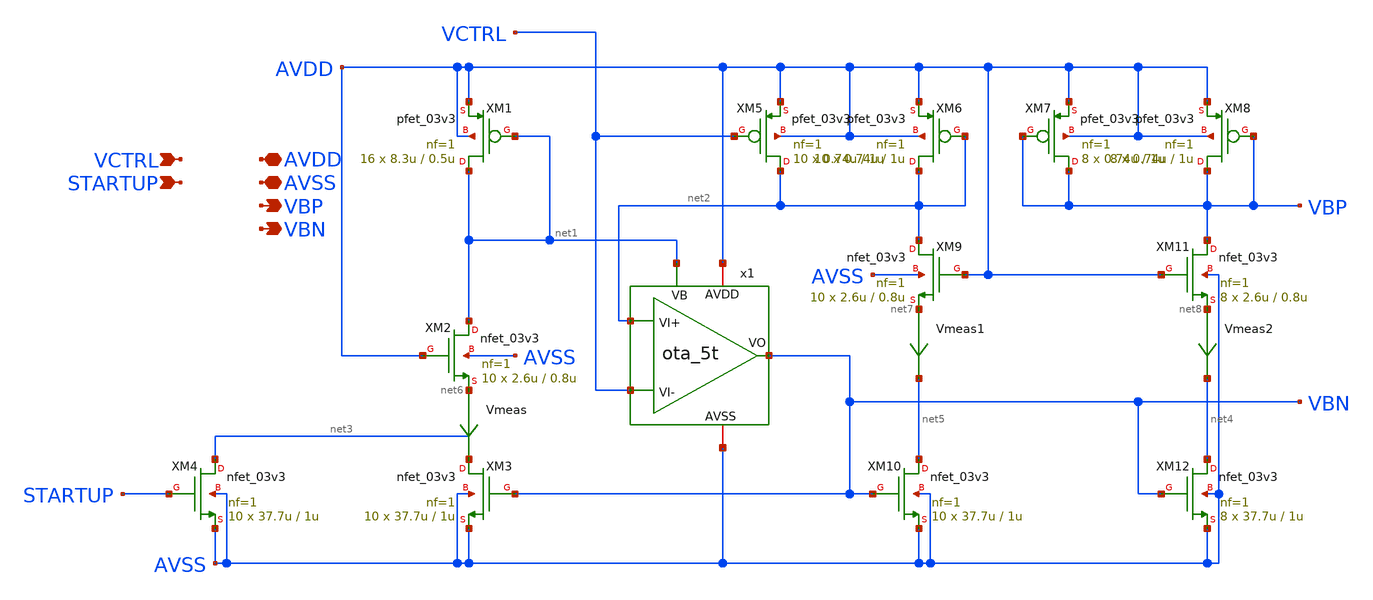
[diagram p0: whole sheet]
** sch_path: designs/libs/core_analog/bias_generator/bias_generator.sch
**.subckt bias_generator VCTRL STARTUP AVDD AVSS VBP VBN
*.ipin VCTRL
*.ipin STARTUP
*.iopin AVDD
*.iopin AVSS
*.opin VBP
*.opin VBN
x1 VBN AVDD net2 VCTRL AVSS net1 ota_5t
XM1 net1 net1 AVDD AVDD pfet_03v3 L=0.5u W=8.3u nf=1 ad='int((nf+1)/2) * W/nf * 0.18u' as='int((nf+2)/2) * W/nf * 0.18u'
+ pd='2*int((nf+1)/2) * (W/nf + 0.18u)' ps='2*int((nf+2)/2) * (W/nf + 0.18u)' nrd='0.18u / W' nrs='0.18u / W'
+ sa=0 sb=0 sd=0 m=16
Vmeas net6 net3 0
.save i(vmeas)
Vmeas1 net7 net5 0
.save i(vmeas1)
Vmeas2 net8 net4 0
.save i(vmeas2)
XM10 net5 VBN AVSS AVSS nfet_03v3 L=1u W=37.7u nf=1 ad='int((nf+1)/2) * W/nf * 0.18u' as='int((nf+2)/2) * W/nf * 0.18u'
+ pd='2*int((nf+1)/2) * (W/nf + 0.18u)' ps='2*int((nf+2)/2) * (W/nf + 0.18u)' nrd='0.18u / W' nrs='0.18u / W'
+ sa=0 sb=0 sd=0 m=10
XM5 net2 VCTRL AVDD AVDD pfet_03v3 L=1u W=0.74u nf=1 ad='int((nf+1)/2) * W/nf * 0.18u' as='int((nf+2)/2) * W/nf * 0.18u'
+ pd='2*int((nf+1)/2) * (W/nf + 0.18u)' ps='2*int((nf+2)/2) * (W/nf + 0.18u)' nrd='0.18u / W' nrs='0.18u / W'
+ sa=0 sb=0 sd=0 m=10
XM9 net2 AVDD net7 AVSS nfet_03v3 L=0.8u W=2.6u nf=1 ad='int((nf+1)/2) * W/nf * 0.18u' as='int((nf+2)/2) * W/nf * 0.18u'
+ pd='2*int((nf+1)/2) * (W/nf + 0.18u)' ps='2*int((nf+2)/2) * (W/nf + 0.18u)' nrd='0.18u / W' nrs='0.18u / W'
+ sa=0 sb=0 sd=0 m=10
XM11 VBP AVDD net8 AVSS nfet_03v3 L=0.8u W=2.6u nf=1 ad='int((nf+1)/2) * W/nf * 0.18u' as='int((nf+2)/2) * W/nf * 0.18u'
+ pd='2*int((nf+1)/2) * (W/nf + 0.18u)' ps='2*int((nf+2)/2) * (W/nf + 0.18u)' nrd='0.18u / W' nrs='0.18u / W'
+ sa=0 sb=0 sd=0 m=8
XM6 net2 net2 AVDD AVDD pfet_03v3 L=1u W=0.74u nf=1 ad='int((nf+1)/2) * W/nf * 0.18u' as='int((nf+2)/2) * W/nf * 0.18u'
+ pd='2*int((nf+1)/2) * (W/nf + 0.18u)' ps='2*int((nf+2)/2) * (W/nf + 0.18u)' nrd='0.18u / W' nrs='0.18u / W'
+ sa=0 sb=0 sd=0 m=10
XM7 VBP VBP AVDD AVDD pfet_03v3 L=1u W=0.74u nf=1 ad='int((nf+1)/2) * W/nf * 0.18u' as='int((nf+2)/2) * W/nf * 0.18u'
+ pd='2*int((nf+1)/2) * (W/nf + 0.18u)' ps='2*int((nf+2)/2) * (W/nf + 0.18u)' nrd='0.18u / W' nrs='0.18u / W'
+ sa=0 sb=0 sd=0 m=8
XM8 VBP VBP AVDD AVDD pfet_03v3 L=1u W=0.74u nf=1 ad='int((nf+1)/2) * W/nf * 0.18u' as='int((nf+2)/2) * W/nf * 0.18u'
+ pd='2*int((nf+1)/2) * (W/nf + 0.18u)' ps='2*int((nf+2)/2) * (W/nf + 0.18u)' nrd='0.18u / W' nrs='0.18u / W'
+ sa=0 sb=0 sd=0 m=8
XM2 net1 AVDD net6 AVSS nfet_03v3 L=0.8u W=2.6u nf=1 ad='int((nf+1)/2) * W/nf * 0.18u' as='int((nf+2)/2) * W/nf * 0.18u'
+ pd='2*int((nf+1)/2) * (W/nf + 0.18u)' ps='2*int((nf+2)/2) * (W/nf + 0.18u)' nrd='0.18u / W' nrs='0.18u / W'
+ sa=0 sb=0 sd=0 m=10
XM12 net4 VBN AVSS AVSS nfet_03v3 L=1u W=37.7u nf=1 ad='int((nf+1)/2) * W/nf * 0.18u' as='int((nf+2)/2) * W/nf * 0.18u'
+ pd='2*int((nf+1)/2) * (W/nf + 0.18u)' ps='2*int((nf+2)/2) * (W/nf + 0.18u)' nrd='0.18u / W' nrs='0.18u / W'
+ sa=0 sb=0 sd=0 m=8
XM3 net3 VBN AVSS AVSS nfet_03v3 L=1u W=37.7u nf=1 ad='int((nf+1)/2) * W/nf * 0.18u' as='int((nf+2)/2) * W/nf * 0.18u'
+ pd='2*int((nf+1)/2) * (W/nf + 0.18u)' ps='2*int((nf+2)/2) * (W/nf + 0.18u)' nrd='0.18u / W' nrs='0.18u / W'
+ sa=0 sb=0 sd=0 m=10
XM4 net3 STARTUP AVSS AVSS nfet_03v3 L=1u W=37.7u nf=1 ad='int((nf+1)/2) * W/nf * 0.18u' as='int((nf+2)/2) * W/nf * 0.18u'
+ pd='2*int((nf+1)/2) * (W/nf + 0.18u)' ps='2*int((nf+2)/2) * (W/nf + 0.18u)' nrd='0.18u / W' nrs='0.18u / W'
+ sa=0 sb=0 sd=0 m=10
**.ends

* expanding   symbol:  libs/core_analog/ota_5t/ota_5t.sym # of pins=6
** sym_path: designs/libs/core_analog/ota_5t/ota_5t.sym
** sch_path: designs/libs/core_analog/ota_5t/ota_5t.sch
.subckt ota_5t VO AVDD VI+ VI- AVSS VB
*.ipin VI+
*.ipin VI-
*.ipin VB
*.iopin AVDD
*.iopin AVSS
*.opin VO
XM1 VO VI- net2 AVDD pfet_03v3 L=0.5u W=6.55u nf=1 ad='int((nf+1)/2) * W/nf * 0.18u' as='int((nf+2)/2) * W/nf * 0.18u'
+ pd='2*int((nf+1)/2) * (W/nf + 0.18u)' ps='2*int((nf+2)/2) * (W/nf + 0.18u)' nrd='0.18u / W' nrs='0.18u / W'
+ sa=0 sb=0 sd=0 m=8
XM4 VO net1 AVSS AVSS nfet_03v3 L=0.5u W=4.8u nf=1 ad='int((nf+1)/2) * W/nf * 0.18u' as='int((nf+2)/2) * W/nf * 0.18u'
+ pd='2*int((nf+1)/2) * (W/nf + 0.18u)' ps='2*int((nf+2)/2) * (W/nf + 0.18u)' nrd='0.18u / W' nrs='0.18u / W'
+ sa=0 sb=0 sd=0 m=4
XM3 net2 VB net3 AVDD pfet_03v3 L=0.5u W=8.3u nf=1 ad='int((nf+1)/2) * W/nf * 0.18u' as='int((nf+2)/2) * W/nf * 0.18u'
+ pd='2*int((nf+1)/2) * (W/nf + 0.18u)' ps='2*int((nf+2)/2) * (W/nf + 0.18u)' nrd='0.18u / W' nrs='0.18u / W'
+ sa=0 sb=0 sd=0 m=16
XM2 net1 VI+ net2 AVDD pfet_03v3 L=0.5u W=6.55u nf=1 ad='int((nf+1)/2) * W/nf * 0.18u' as='int((nf+2)/2) * W/nf * 0.18u'
+ pd='2*int((nf+1)/2) * (W/nf + 0.18u)' ps='2*int((nf+2)/2) * (W/nf + 0.18u)' nrd='0.18u / W' nrs='0.18u / W'
+ sa=0 sb=0 sd=0 m=8
XM5 net1 net1 AVSS AVSS nfet_03v3 L=0.5u W=4.8u nf=1 ad='int((nf+1)/2) * W/nf * 0.18u' as='int((nf+2)/2) * W/nf * 0.18u'
+ pd='2*int((nf+1)/2) * (W/nf + 0.18u)' ps='2*int((nf+2)/2) * (W/nf + 0.18u)' nrd='0.18u / W' nrs='0.18u / W'
+ sa=0 sb=0 sd=0 m=4
Vmeas AVDD net3 0
.save i(vmeas)
.ends

.end
